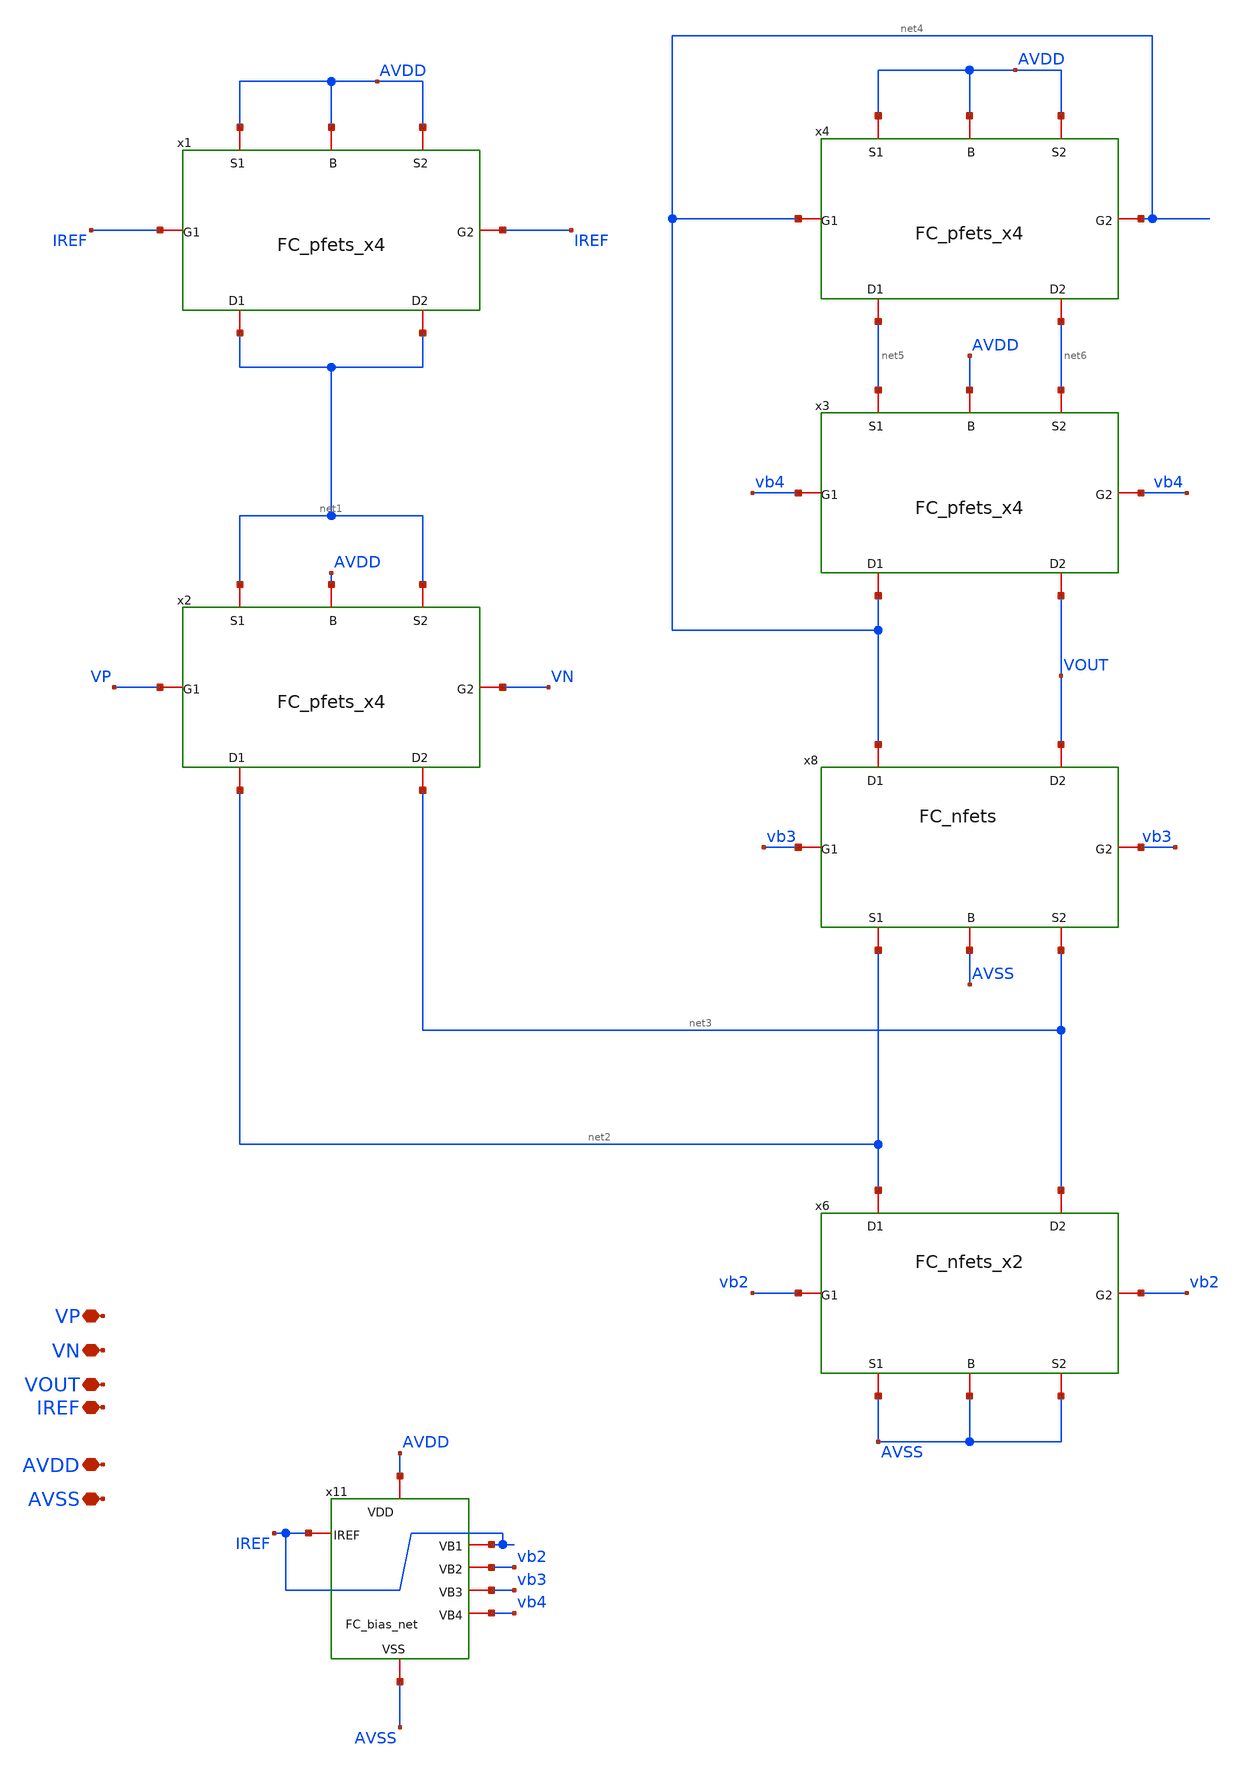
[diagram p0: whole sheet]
** sch_path: Voltage_Reference/LDO/Folded/FC_top.sch
**.subckt FC_top AVDD AVSS VOUT VP VN IREF
*.iopin AVDD
*.iopin AVSS
*.iopin VOUT
*.iopin VP
*.iopin VN
*.iopin IREF
x1 AVDD AVDD net1 net1 IREF IREF AVDD FC_pfets_x4
x2 net1 net1 net2 net3 VP VN AVDD FC_pfets_x4
x3 net5 net6 net4 VOUT vb4 vb4 AVDD FC_pfets_x4
x4 AVDD AVDD net5 net6 net4 net4 AVDD FC_pfets_x4
x11 IREF IREF vb2 vb3 vb4 AVDD AVSS FC_bias_net
x6 AVSS AVSS net2 net3 vb2 vb2 AVSS FC_nfets_x2
x8 net2 net3 net4 VOUT vb3 vb3 AVSS FC_nfets
**.ends
.end
